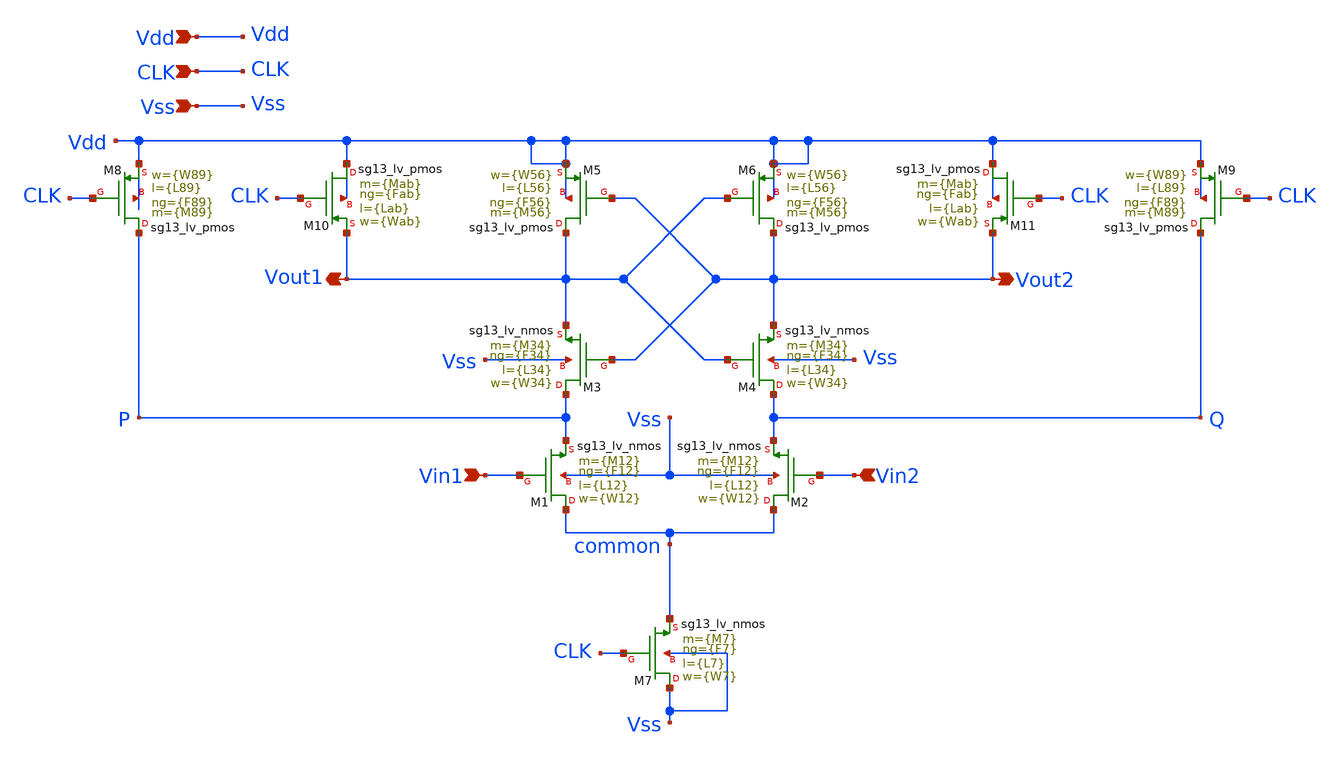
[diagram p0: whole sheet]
** sch_path: xschem/sch/strongarm.sch
**.subckt strongarm Vout2 Vout1 Vin1 Vin2 CLK Vss Vdd
*.opin Vout2
*.opin Vout1
*.ipin Vin1
*.ipin Vin2
*.ipin CLK
*.ipin Vss
*.ipin Vdd
XM1 common Vin1 P Vss sg13_lv_nmos w={W12} l={L12} ng={F12} m={M12} mm_ok=1
XM2 common Vin2 Q Vss sg13_lv_nmos w={W12} l={L12} ng={F12} m={M12} mm_ok=1
XM3 P Vout2 Vout1 Vss sg13_lv_nmos w={W34} l={L34} ng={F34} m={M34} mm_ok=1
XM4 Q Vout1 Vout2 Vss sg13_lv_nmos w={W34} l={L34} ng={F34} m={M34} mm_ok=1
XM6 Vout2 Vout1 Vdd Vdd sg13_lv_pmos w={W56} l={L56} ng={F56} m={M56} mm_ok=1
XM5 Vout1 Vout2 Vdd Vdd sg13_lv_pmos w={W56} l={L56} ng={F56} m={M56} mm_ok=1
XM7 Vss CLK common Vss sg13_lv_nmos w={W7} l={L7} ng={F7} m={M7} mm_ok=1
XM8 P CLK Vdd Vdd sg13_lv_pmos w={W89} l={L89} ng={F89} m={M89} mm_ok=1
XM9 Q CLK Vdd Vdd sg13_lv_pmos w={W89} l={L89} ng={F89} m={M89} mm_ok=1
XM11 Vdd CLK Vout2 Vdd sg13_lv_pmos w={Wab} l={Lab} ng={Fab} m={Mab} mm_ok=1
XM10 Vdd CLK Vout1 Vdd sg13_lv_pmos w={Wab} l={Lab} ng={Fab} m={Mab} mm_ok=1
**.ends
.end
